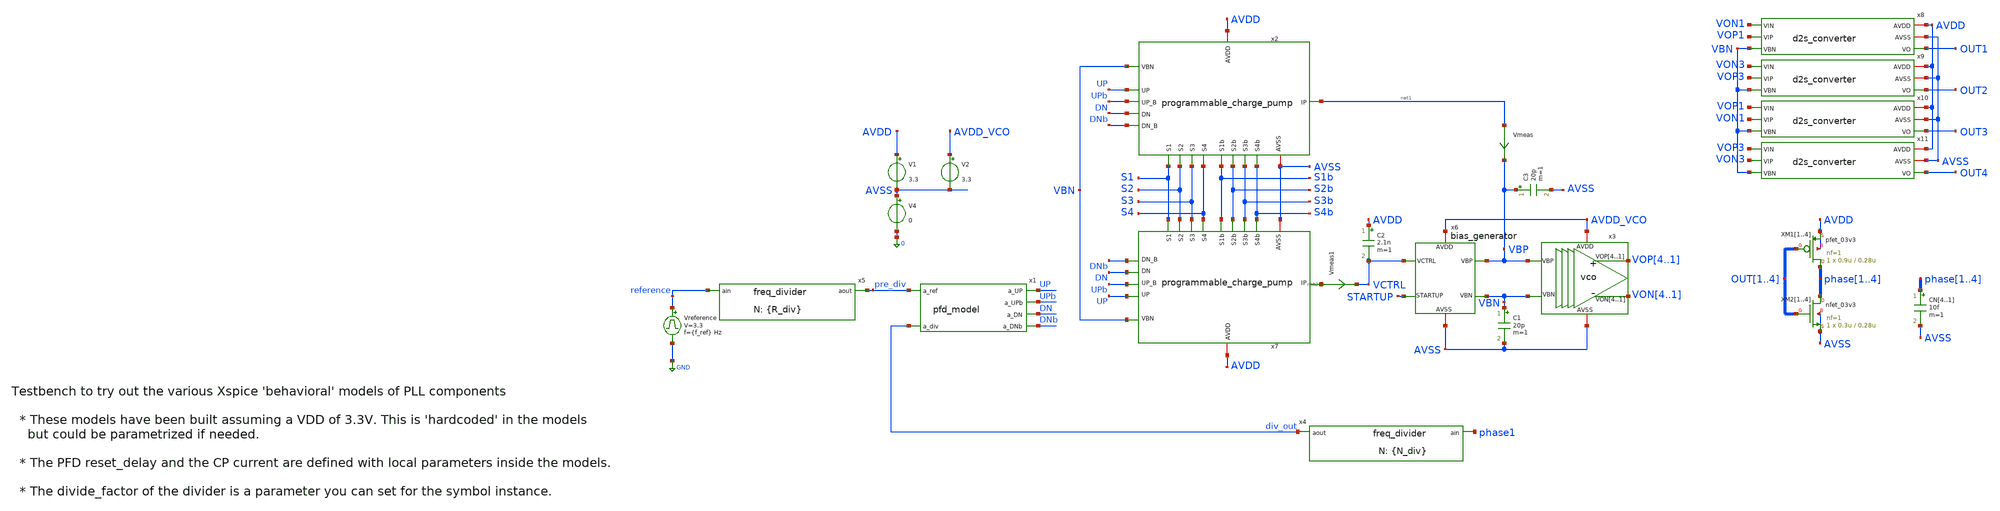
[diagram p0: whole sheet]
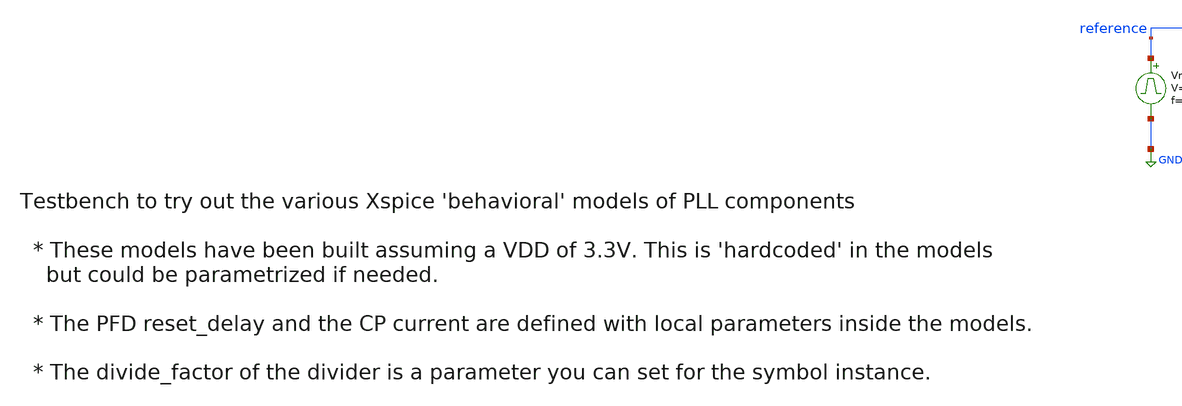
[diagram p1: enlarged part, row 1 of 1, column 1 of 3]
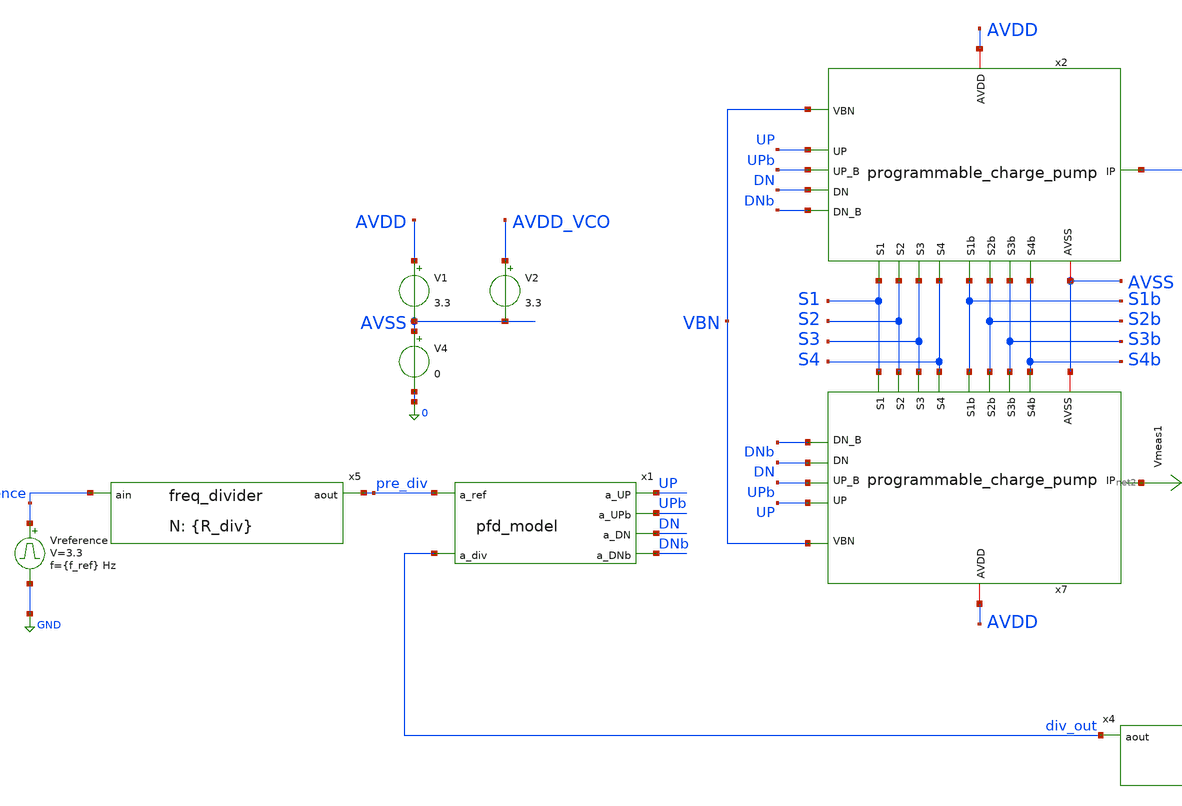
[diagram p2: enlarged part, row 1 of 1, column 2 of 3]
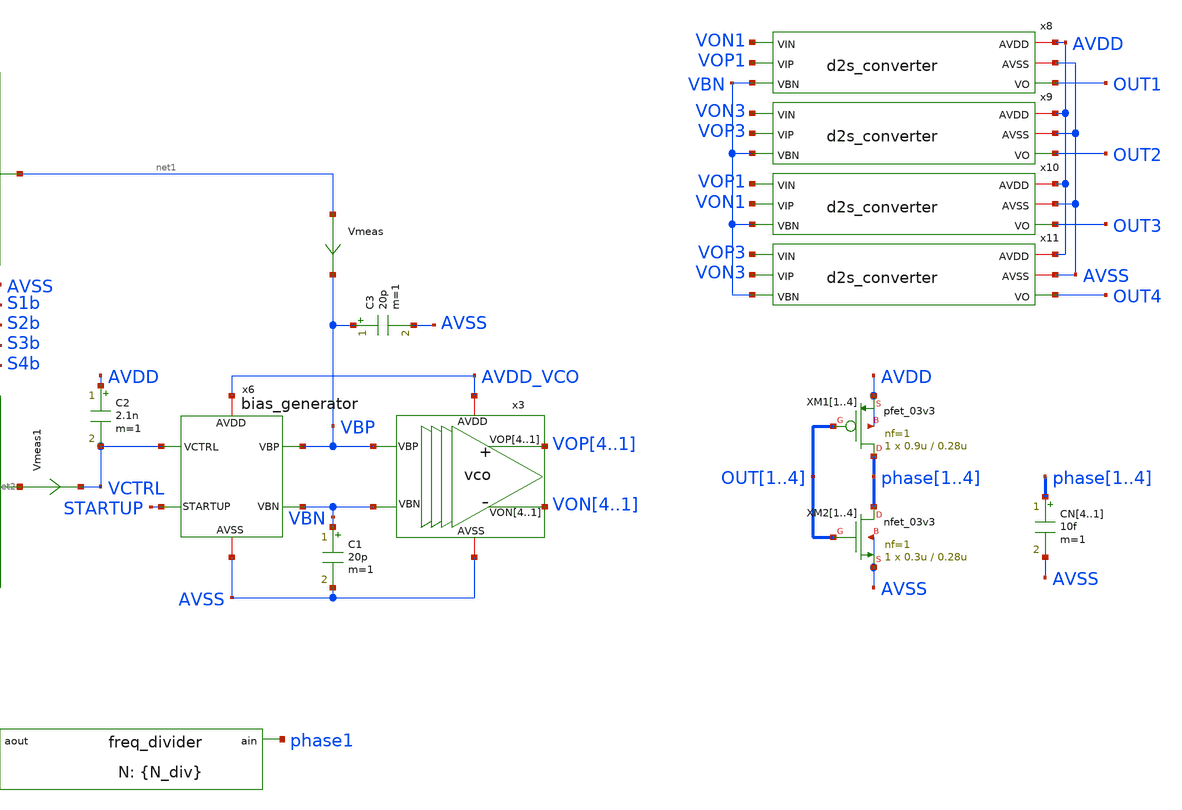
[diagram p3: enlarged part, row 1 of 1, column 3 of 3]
** sch_path: designs/libs/tb_pll/tb_PLL_CP_VCO_model.sch
**.subckt tb_PLL_CP_VCO_model
Vreference reference GND pulse 0 3.3 '0.495/ {f_ref} ' '0.01/{f_ref} ' '0.01/{f_ref} ' '0.49/{f_ref} '
+ '1/{f_ref} '
x1 pre_div UP UPb DN div_out DNb pfd_model
x4 div_out phase1 freq_divider divide_factor={N_div}
x5 pre_div reference freq_divider divide_factor={R_div}
x3 VOP4 VOP3 VOP2 VOP1 VON4 VON3 VON2 VON1 AVDD_VCO AVSS VBP VBN vco
x6 VCTRL AVDD_VCO STARTUP AVSS VBP VBN bias_generator
C2 AVDD VCTRL 2.1n m=1
x8 AVDD AVSS VON1 VOP1 VBN OUT1 d2s_converter
XM11 phase1 OUT1 AVDD AVDD pfet_03v3 L=0.28u W=0.9u nf=1 ad='int((nf+1)/2) * W/nf * 0.18u' as='int((nf+2)/2) * W/nf * 0.18u'
+ pd='2*int((nf+1)/2) * (W/nf + 0.18u)' ps='2*int((nf+2)/2) * (W/nf + 0.18u)' nrd='0.18u / W' nrs='0.18u / W'
+ sa=0 sb=0 sd=0 m=1
XM12 phase2 OUT2 AVDD AVDD pfet_03v3 L=0.28u W=0.9u nf=1 ad='int((nf+1)/2) * W/nf * 0.18u' as='int((nf+2)/2) * W/nf * 0.18u'
+ pd='2*int((nf+1)/2) * (W/nf + 0.18u)' ps='2*int((nf+2)/2) * (W/nf + 0.18u)' nrd='0.18u / W' nrs='0.18u / W'
+ sa=0 sb=0 sd=0 m=1
XM13 phase3 OUT3 AVDD AVDD pfet_03v3 L=0.28u W=0.9u nf=1 ad='int((nf+1)/2) * W/nf * 0.18u' as='int((nf+2)/2) * W/nf * 0.18u'
+ pd='2*int((nf+1)/2) * (W/nf + 0.18u)' ps='2*int((nf+2)/2) * (W/nf + 0.18u)' nrd='0.18u / W' nrs='0.18u / W'
+ sa=0 sb=0 sd=0 m=1
XM14 phase4 OUT4 AVDD AVDD pfet_03v3 L=0.28u W=0.9u nf=1 ad='int((nf+1)/2) * W/nf * 0.18u' as='int((nf+2)/2) * W/nf * 0.18u'
+ pd='2*int((nf+1)/2) * (W/nf + 0.18u)' ps='2*int((nf+2)/2) * (W/nf + 0.18u)' nrd='0.18u / W' nrs='0.18u / W'
+ sa=0 sb=0 sd=0 m=1
XM21 phase1 OUT1 AVSS AVSS nfet_03v3 L=0.28u W=0.3u nf=1 ad='int((nf+1)/2) * W/nf * 0.18u' as='int((nf+2)/2) * W/nf * 0.18u'
+ pd='2*int((nf+1)/2) * (W/nf + 0.18u)' ps='2*int((nf+2)/2) * (W/nf + 0.18u)' nrd='0.18u / W' nrs='0.18u / W'
+ sa=0 sb=0 sd=0 m=1
XM22 phase2 OUT2 AVSS AVSS nfet_03v3 L=0.28u W=0.3u nf=1 ad='int((nf+1)/2) * W/nf * 0.18u' as='int((nf+2)/2) * W/nf * 0.18u'
+ pd='2*int((nf+1)/2) * (W/nf + 0.18u)' ps='2*int((nf+2)/2) * (W/nf + 0.18u)' nrd='0.18u / W' nrs='0.18u / W'
+ sa=0 sb=0 sd=0 m=1
XM23 phase3 OUT3 AVSS AVSS nfet_03v3 L=0.28u W=0.3u nf=1 ad='int((nf+1)/2) * W/nf * 0.18u' as='int((nf+2)/2) * W/nf * 0.18u'
+ pd='2*int((nf+1)/2) * (W/nf + 0.18u)' ps='2*int((nf+2)/2) * (W/nf + 0.18u)' nrd='0.18u / W' nrs='0.18u / W'
+ sa=0 sb=0 sd=0 m=1
XM24 phase4 OUT4 AVSS AVSS nfet_03v3 L=0.28u W=0.3u nf=1 ad='int((nf+1)/2) * W/nf * 0.18u' as='int((nf+2)/2) * W/nf * 0.18u'
+ pd='2*int((nf+1)/2) * (W/nf + 0.18u)' ps='2*int((nf+2)/2) * (W/nf + 0.18u)' nrd='0.18u / W' nrs='0.18u / W'
+ sa=0 sb=0 sd=0 m=1
x9 AVDD AVSS VON3 VOP3 VBN OUT2 d2s_converter
x10 AVDD AVSS VOP1 VON1 VBN OUT3 d2s_converter
x11 AVDD AVSS VOP3 VON3 VBN OUT4 d2s_converter
V1 AVDD AVSS 3.3
V4 AVSS 0 0
V2 AVDD_VCO AVSS 3.3
x2 AVSS AVDD UP UPb DN net1 DNb VBN S1b S1 S2b S2 S3b S3 S4b S4 programmable_charge_pump
x7 AVSS AVDD UP UPb DN net2 DNb VBN S1b S1 S2b S2 S3b S3 S4b S4 programmable_charge_pump
CN4 phase1 AVSS 10f m=1
CN3 phase2 AVSS 10f m=1
CN2 phase3 AVSS 10f m=1
CN1 phase4 AVSS 10f m=1
Vmeas net1 VBP 0
.save i(vmeas)
Vmeas1 net2 VCTRL 0
.save i(vmeas1)
C1 VBN AVSS 20p m=1
C3 VBP AVSS 20p m=1
**** begin user architecture code


.param f_ref=2e3 R_div=2 N_div=255
.ic v(vop1)=3.3 v(von1)=0 v(startup)=0 v(VCTRL)=2.65 v(vbp)=2.65
.options reltol=1e-2 cshunt=1e-15
.options method=gear

.param d1=0 d2=0 d3=0 d4=0
.param d1b=3.3 d2b=3.3 d3b=3.3 d4b=3.3

*.param d1=3.3 d2=3.3 d3=3.3 d4=3.3
*.param d1b=0 d2b=0 d3b=0 d4b=0

VS1 S1 0 d1
VS2 S2 0 d2
VS3 S3 0 d3
VS4 S4 0 d4

VS1b S1b 0 d1b
VS2b S2b 0 d2b
VS3b S3b 0 d3b
VS4b S4b 0 d4b

.control

* save all
save v(VCTRL) v(vbp) v(vbn) v(vop1) v(von1) v(vop3) v(von3) v(reference) v(div_out) v(pre_div)
+ v(phase1) v(phase2) v(phase3) v(phase4) v(up) v(dn)

OP
show all

tran 100n 50m

remzerovec

*write tb_PLL_CP_VCO_model_350MEG.raw
*write tb_PLL_CP_VCO_model_R2_N256_256MEG.raw

*write tb_PLL_CP_VCO_model_R2_N2_350MEG.raw *tran 1
*write tb_PLL_CP_VCO_model_R2_N255_255MEG.raw *tran 2

*tran 3
*write tb_PLL_CP_VCO_model_R2_N2_50kHz.raw
*tran 4
write tb_PLL_CP_VCO_model_R2_N255_255kHz.raw
.endc



.include $::180MCU_MODELS/design.ngspice
.lib $::180MCU_MODELS/sm141064.ngspice typical
*.lib $::180MCU_MODELS/sm141064.ngspice SS
*.lib $::180MCU_MODELS/sm141064.ngspice FF
*.lib $::180MCU_MODELS/sm141064.ngspice SF
*.lib $::180MCU_MODELS/sm141064.ngspice FS

**** end user architecture code
**.ends
.GLOBAL GND
.end
